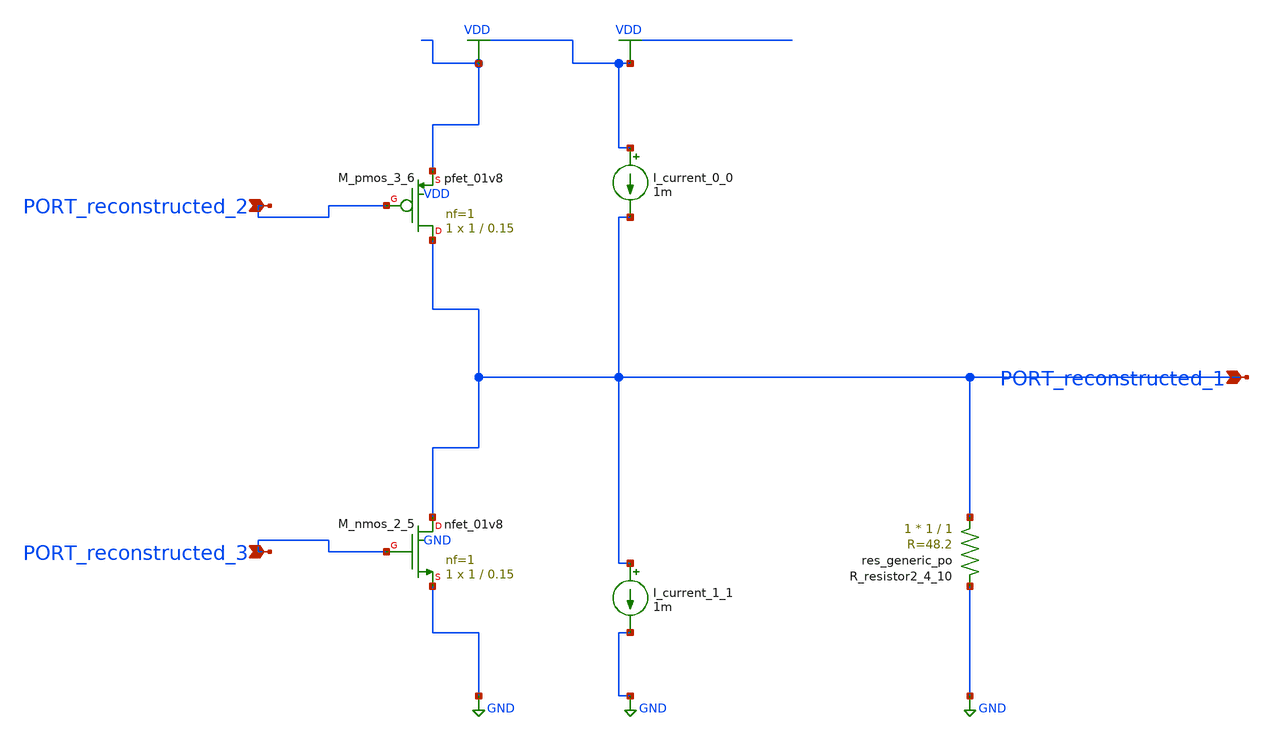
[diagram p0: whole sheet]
** sch_path: schematics/AMSNet/459.sch
**.subckt 459 PORT_reconstructed_1 PORT_reconstructed_2 PORT_reconstructed_3
*.ipin PORT_reconstructed_1
*.ipin PORT_reconstructed_2
*.ipin PORT_reconstructed_3
I_current_0_0 VDD PORT_reconstructed_1 1m
I_current_1_1 PORT_reconstructed_1 GND 1m
XM_nmos_2_5 PORT_reconstructed_1 PORT_reconstructed_3 GND GND sky130_fd_pr__nfet_01v8 L=0.15 W=1 nf=1
+ ad='int((1 + 1)/2) * 1 / 1 * 0.29' as='int((1 + 2)/2) * 1 / 1 * 0.29' pd='2*int((1 + 1)/2) * (1 / 1 + 0.29)'
+ ps='2*int((1 + 2)/2) * (1 / 1 + 0.29)' nrd='0.29 / 1 ' nrs='0.29 / 1 ' sa=0 sb=0 sd=0 mult=1 m=1
XM_pmos_3_6 PORT_reconstructed_1 PORT_reconstructed_2 VDD VDD sky130_fd_pr__pfet_01v8 L=0.15 W=1 nf=1
+ ad='int((1 + 1)/2) * 1 / 1 * 0.29' as='int((1 + 2)/2) * 1 / 1 * 0.29' pd='2*int((1 + 1)/2) * (1 / 1 + 0.29)'
+ ps='2*int((1 + 2)/2) * (1 / 1 + 0.29)' nrd='0.29 / 1 ' nrs='0.29 / 1 ' sa=0 sb=0 sd=0 mult=1 m=1
XR_resistor2_4_10 PORT_reconstructed_1 GND sky130_fd_pr__res_generic_po W=1 L=1 m=1
**.ends
.GLOBAL GND
.GLOBAL VDD
.end
